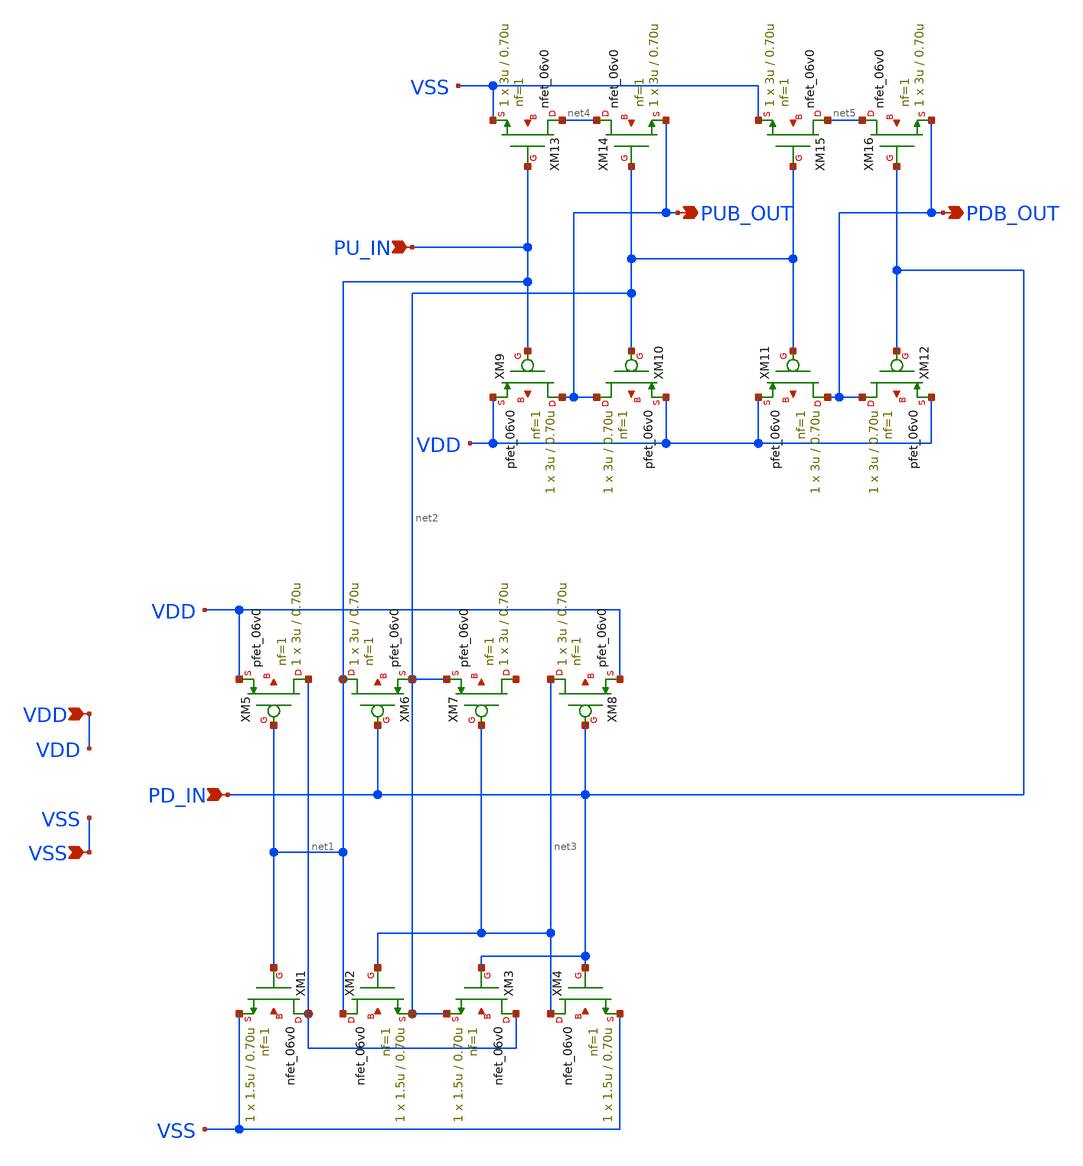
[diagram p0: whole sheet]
** sch_path: gf180mcu_fd_io__bi_24t/comp018green_in_logic_pupd.sch
**.subckt comp018green_in_logic_pupd VDD VSS PD_IN PU_IN PUB_OUT PDB_OUT
*.ipin VDD
*.ipin VSS
*.ipin PD_IN
*.ipin PU_IN
*.opin PUB_OUT
*.opin PDB_OUT
XM1 net1 PU_IN VSS net6 nfet_06v0 L=0.70u W=1.5u nf=1 ad='int((nf+1)/2) * W/nf * 0.18u' as='int((nf+2)/2) * W/nf * 0.18u'
+ pd='2*int((nf+1)/2) * (W/nf + 0.18u)' ps='2*int((nf+2)/2) * (W/nf + 0.18u)' nrd='0.18u / W' nrs='0.18u / W'
+ sa=0 sb=0 sd=0 m=1
XM2 PU_IN net3 net2 net7 nfet_06v0 L=0.70u W=1.5u nf=1 ad='int((nf+1)/2) * W/nf * 0.18u' as='int((nf+2)/2) * W/nf * 0.18u'
+ pd='2*int((nf+1)/2) * (W/nf + 0.18u)' ps='2*int((nf+2)/2) * (W/nf + 0.18u)' nrd='0.18u / W' nrs='0.18u / W'
+ sa=0 sb=0 sd=0 m=1
XM3 net1 PD_IN net2 net8 nfet_06v0 L=0.70u W=1.5u nf=1 ad='int((nf+1)/2) * W/nf * 0.18u' as='int((nf+2)/2) * W/nf * 0.18u'
+ pd='2*int((nf+1)/2) * (W/nf + 0.18u)' ps='2*int((nf+2)/2) * (W/nf + 0.18u)' nrd='0.18u / W' nrs='0.18u / W'
+ sa=0 sb=0 sd=0 m=1
XM4 net3 PD_IN VSS net9 nfet_06v0 L=0.70u W=1.5u nf=1 ad='int((nf+1)/2) * W/nf * 0.18u' as='int((nf+2)/2) * W/nf * 0.18u'
+ pd='2*int((nf+1)/2) * (W/nf + 0.18u)' ps='2*int((nf+2)/2) * (W/nf + 0.18u)' nrd='0.18u / W' nrs='0.18u / W'
+ sa=0 sb=0 sd=0 m=1
XM5 net1 PU_IN VDD net10 pfet_06v0 L=0.70u W=3u nf=1 ad='int((nf+1)/2) * W/nf * 0.18u' as='int((nf+2)/2) * W/nf * 0.18u'
+ pd='2*int((nf+1)/2) * (W/nf + 0.18u)' ps='2*int((nf+2)/2) * (W/nf + 0.18u)' nrd='0.18u / W' nrs='0.18u / W'
+ sa=0 sb=0 sd=0 m=1
XM6 PU_IN PD_IN net2 net11 pfet_06v0 L=0.70u W=3u nf=1 ad='int((nf+1)/2) * W/nf * 0.18u' as='int((nf+2)/2) * W/nf * 0.18u'
+ pd='2*int((nf+1)/2) * (W/nf + 0.18u)' ps='2*int((nf+2)/2) * (W/nf + 0.18u)' nrd='0.18u / W' nrs='0.18u / W'
+ sa=0 sb=0 sd=0 m=1
XM7 net12 net3 net2 net13 pfet_06v0 L=0.70u W=3u nf=1 ad='int((nf+1)/2) * W/nf * 0.18u' as='int((nf+2)/2) * W/nf * 0.18u'
+ pd='2*int((nf+1)/2) * (W/nf + 0.18u)' ps='2*int((nf+2)/2) * (W/nf + 0.18u)' nrd='0.18u / W' nrs='0.18u / W'
+ sa=0 sb=0 sd=0 m=1
XM8 net3 PD_IN VDD net14 pfet_06v0 L=0.70u W=3u nf=1 ad='int((nf+1)/2) * W/nf * 0.18u' as='int((nf+2)/2) * W/nf * 0.18u'
+ pd='2*int((nf+1)/2) * (W/nf + 0.18u)' ps='2*int((nf+2)/2) * (W/nf + 0.18u)' nrd='0.18u / W' nrs='0.18u / W'
+ sa=0 sb=0 sd=0 m=1
XM9 PUB_OUT PU_IN VDD net15 pfet_06v0 L=0.70u W=3u nf=1 ad='int((nf+1)/2) * W/nf * 0.18u' as='int((nf+2)/2) * W/nf * 0.18u'
+ pd='2*int((nf+1)/2) * (W/nf + 0.18u)' ps='2*int((nf+2)/2) * (W/nf + 0.18u)' nrd='0.18u / W' nrs='0.18u / W'
+ sa=0 sb=0 sd=0 m=1
XM10 PUB_OUT net2 VDD net16 pfet_06v0 L=0.70u W=3u nf=1 ad='int((nf+1)/2) * W/nf * 0.18u' as='int((nf+2)/2) * W/nf * 0.18u'
+ pd='2*int((nf+1)/2) * (W/nf + 0.18u)' ps='2*int((nf+2)/2) * (W/nf + 0.18u)' nrd='0.18u / W' nrs='0.18u / W'
+ sa=0 sb=0 sd=0 m=1
XM11 PDB_OUT net2 VDD net17 pfet_06v0 L=0.70u W=3u nf=1 ad='int((nf+1)/2) * W/nf * 0.18u' as='int((nf+2)/2) * W/nf * 0.18u'
+ pd='2*int((nf+1)/2) * (W/nf + 0.18u)' ps='2*int((nf+2)/2) * (W/nf + 0.18u)' nrd='0.18u / W' nrs='0.18u / W'
+ sa=0 sb=0 sd=0 m=1
XM12 PDB_OUT PD_IN VDD net18 pfet_06v0 L=0.70u W=3u nf=1 ad='int((nf+1)/2) * W/nf * 0.18u' as='int((nf+2)/2) * W/nf * 0.18u'
+ pd='2*int((nf+1)/2) * (W/nf + 0.18u)' ps='2*int((nf+2)/2) * (W/nf + 0.18u)' nrd='0.18u / W' nrs='0.18u / W'
+ sa=0 sb=0 sd=0 m=1
XM13 net4 PU_IN VSS net19 nfet_06v0 L=0.70u W=3u nf=1 ad='int((nf+1)/2) * W/nf * 0.18u' as='int((nf+2)/2) * W/nf * 0.18u'
+ pd='2*int((nf+1)/2) * (W/nf + 0.18u)' ps='2*int((nf+2)/2) * (W/nf + 0.18u)' nrd='0.18u / W' nrs='0.18u / W'
+ sa=0 sb=0 sd=0 m=1
XM14 net4 net2 PUB_OUT net20 nfet_06v0 L=0.70u W=3u nf=1 ad='int((nf+1)/2) * W/nf * 0.18u' as='int((nf+2)/2) * W/nf * 0.18u'
+ pd='2*int((nf+1)/2) * (W/nf + 0.18u)' ps='2*int((nf+2)/2) * (W/nf + 0.18u)' nrd='0.18u / W' nrs='0.18u / W'
+ sa=0 sb=0 sd=0 m=1
XM15 net5 net2 VSS net21 nfet_06v0 L=0.70u W=3u nf=1 ad='int((nf+1)/2) * W/nf * 0.18u' as='int((nf+2)/2) * W/nf * 0.18u'
+ pd='2*int((nf+1)/2) * (W/nf + 0.18u)' ps='2*int((nf+2)/2) * (W/nf + 0.18u)' nrd='0.18u / W' nrs='0.18u / W'
+ sa=0 sb=0 sd=0 m=1
XM16 net5 PD_IN PDB_OUT net22 nfet_06v0 L=0.70u W=3u nf=1 ad='int((nf+1)/2) * W/nf * 0.18u' as='int((nf+2)/2) * W/nf * 0.18u'
+ pd='2*int((nf+1)/2) * (W/nf + 0.18u)' ps='2*int((nf+2)/2) * (W/nf + 0.18u)' nrd='0.18u / W' nrs='0.18u / W'
+ sa=0 sb=0 sd=0 m=1
**.ends
.end
